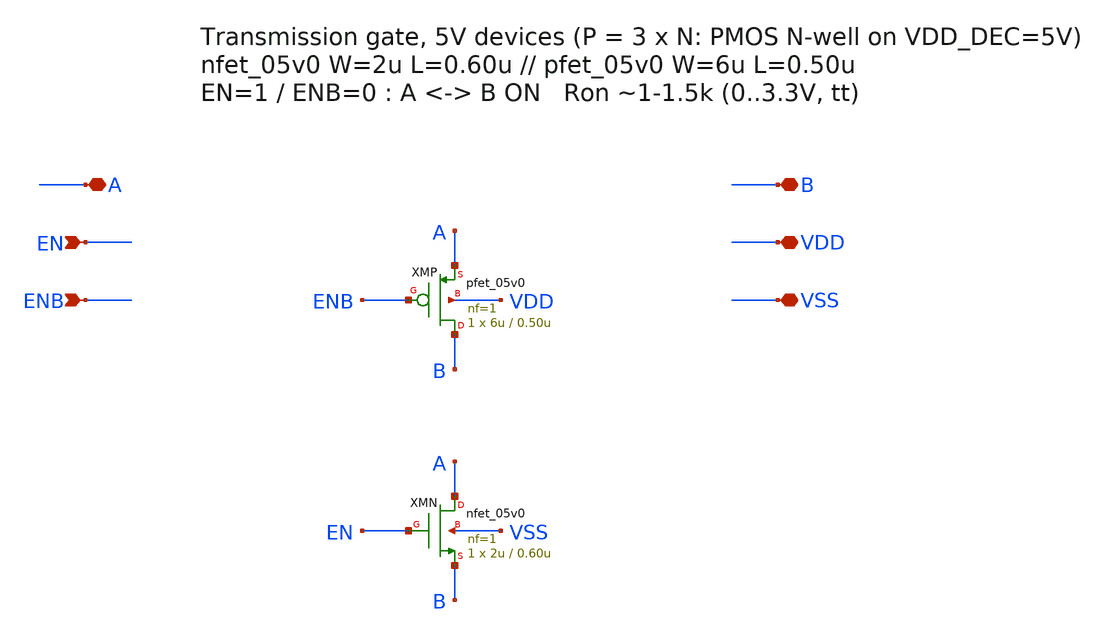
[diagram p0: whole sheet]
** sch_path: inverter_matrix/tgate_5v0.sch
**.subckt tgate_5v0 A B EN ENB VDD VSS
*.iopin A
*.iopin B
*.ipin EN
*.ipin ENB
*.iopin VDD
*.iopin VSS
XMN A EN B VSS nfet_05v0 L=0.60u W=2u nf=1 ad='int((nf+1)/2) * W/nf * 0.18u' as='int((nf+2)/2) * W/nf * 0.18u'
+ pd='2*int((nf+1)/2) * (W/nf + 0.18u)' ps='2*int((nf+2)/2) * (W/nf + 0.18u)' nrd='0.18u / W' nrs='0.18u / W'
+ sa=0 sb=0 sd=0 m=1
XMP B ENB A VDD pfet_05v0 L=0.50u W=6u nf=1 ad='int((nf+1)/2) * W/nf * 0.18u' as='int((nf+2)/2) * W/nf * 0.18u'
+ pd='2*int((nf+1)/2) * (W/nf + 0.18u)' ps='2*int((nf+2)/2) * (W/nf + 0.18u)' nrd='0.18u / W' nrs='0.18u / W'
+ sa=0 sb=0 sd=0 m=1
**.ends
.end
